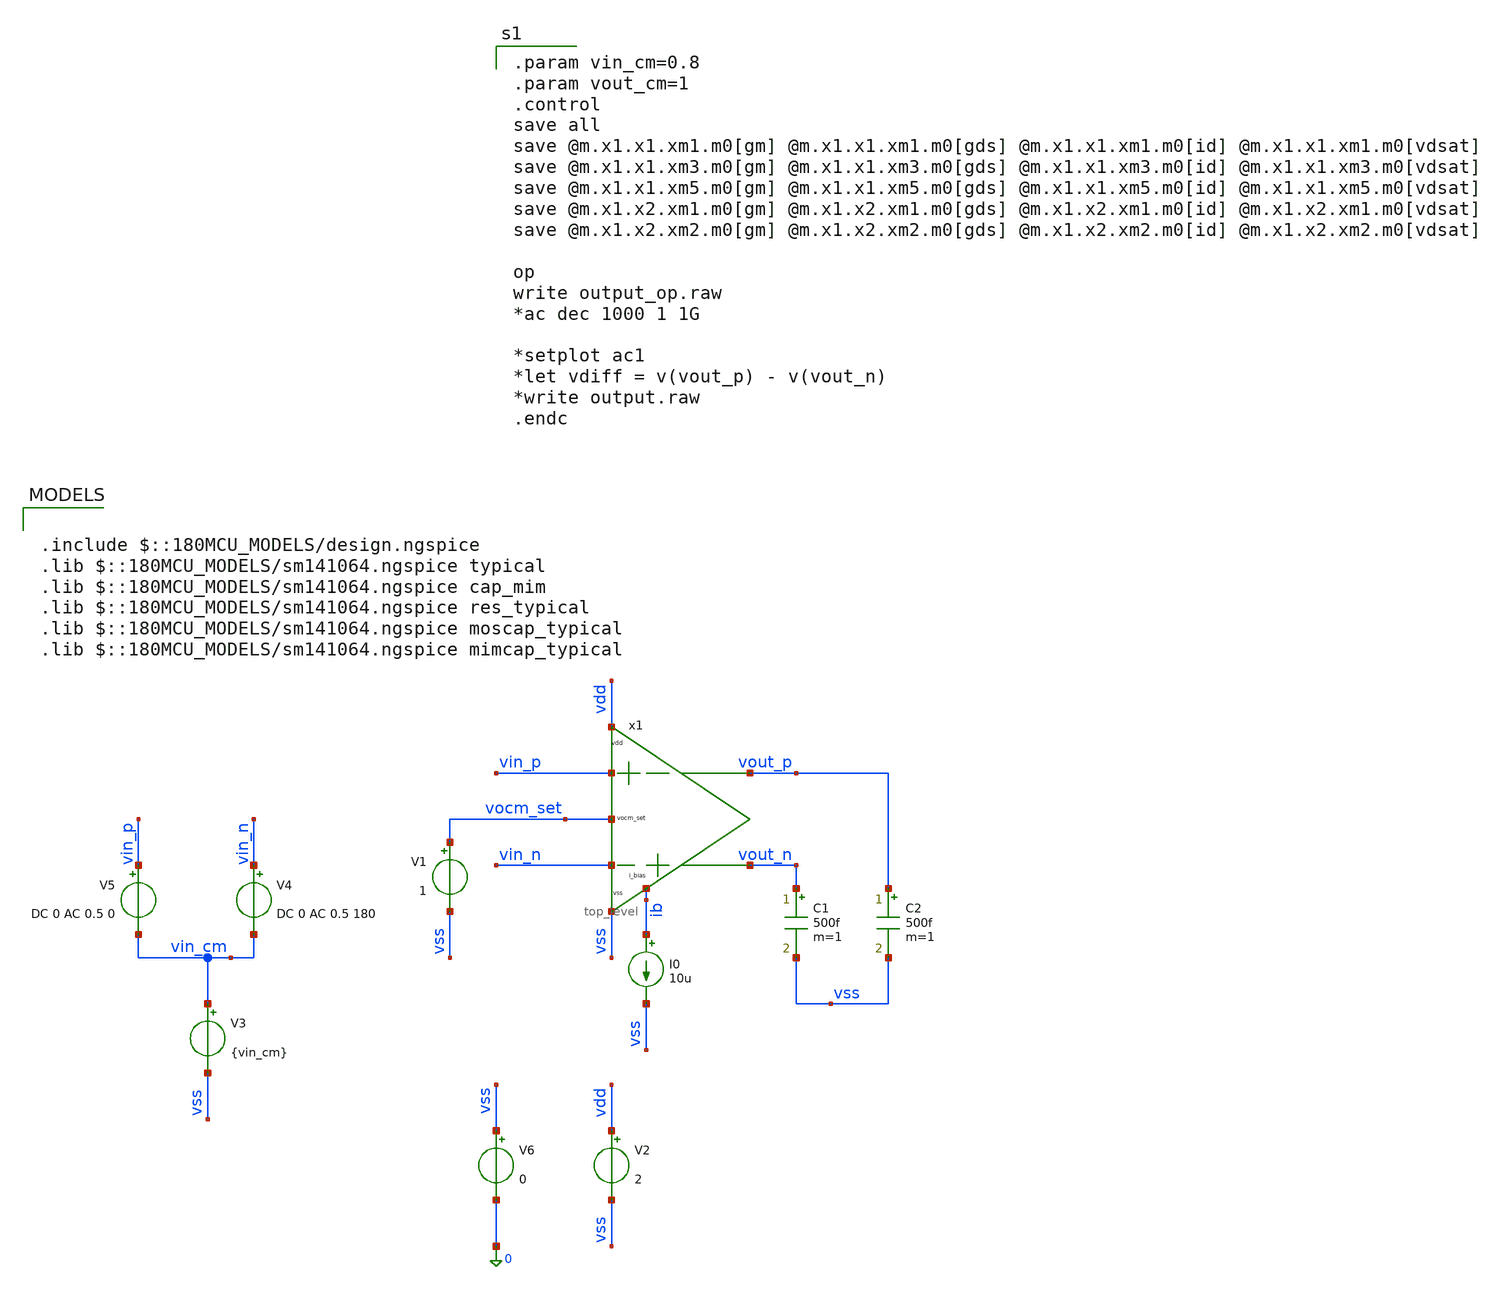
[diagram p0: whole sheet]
** sch_path: xschem/top_level/top_level_tb.sch
**.subckt top_level_tb
x1 vdd vss vin_p vin_n vout_n vout_p vocm_set ib top_level
C1 vout_n vss 500f m=1
C2 vout_p vss 500f m=1
I0 ib vss 10u
V1 vocm_set vss 1
V3 vin_cm vss {vin_cm}
V5 vin_p vin_cm DC 0 AC 0.5 0
V4 vin_n vin_cm DC 0 AC 0.5 180
V2 vdd vss 2
V6 vss 0 0
**** begin user architecture code

.param vin_cm=0.8
.param vout_cm=1
.control
save all
save @m.x1.x1.xm1.m0[gm] @m.x1.x1.xm1.m0[gds] @m.x1.x1.xm1.m0[id] @m.x1.x1.xm1.m0[vdsat]
save @m.x1.x1.xm3.m0[gm] @m.x1.x1.xm3.m0[gds] @m.x1.x1.xm3.m0[id] @m.x1.x1.xm3.m0[vdsat]
save @m.x1.x1.xm5.m0[gm] @m.x1.x1.xm5.m0[gds] @m.x1.x1.xm5.m0[id] @m.x1.x1.xm5.m0[vdsat]
save @m.x1.x2.xm1.m0[gm] @m.x1.x2.xm1.m0[gds] @m.x1.x2.xm1.m0[id] @m.x1.x2.xm1.m0[vdsat]
save @m.x1.x2.xm2.m0[gm] @m.x1.x2.xm2.m0[gds] @m.x1.x2.xm2.m0[id] @m.x1.x2.xm2.m0[vdsat]

op
write output_op.raw
*ac dec 1000 1 1G

*setplot ac1
*let vdiff = v(vout_p) - v(vout_n)
*write output.raw
.endc


.include $::180MCU_MODELS/design.ngspice
.lib $::180MCU_MODELS/sm141064.ngspice typical
.lib $::180MCU_MODELS/sm141064.ngspice cap_mim
.lib $::180MCU_MODELS/sm141064.ngspice res_typical
.lib $::180MCU_MODELS/sm141064.ngspice moscap_typical
.lib $::180MCU_MODELS/sm141064.ngspice mimcap_typical

**** end user architecture code
**.ends
.end
